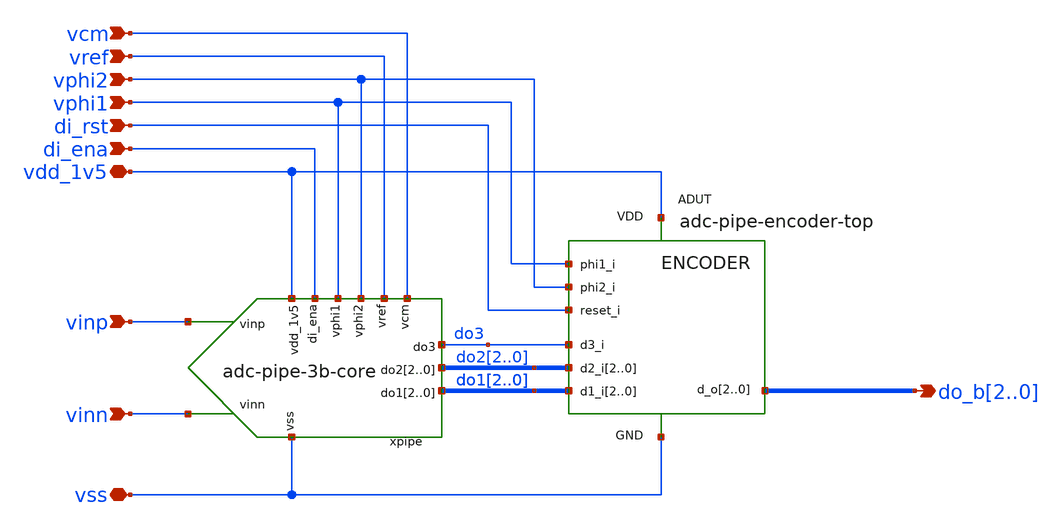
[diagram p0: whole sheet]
** sch_path: xschem/adc-pipe-3b-top.sch
* xschem/ota-5t-fd.sch:
* (c) 2025 M. Koefinger
**.subckt adc-pipe-3b-top vinp vinn di_rst di_ena vphi1 vphi2 vref vcm vdd_1v5 vss do_b2,do_b1,do_b0
*.ipin vinp
*.ipin vinn
*.ipin di_rst
*.ipin di_ena
*.ipin vphi1
*.ipin vphi2
*.ipin vref
*.ipin vcm
*.iopin vdd_1v5
*.iopin vss
*.opin do_b2,do_b1,do_b0
xpipe di_ena vphi2 vphi1 vcm vref vdd_1v5 vinp vinn do3 do22 do21 do20 do12 do11 do10 vss
+ adc-pipe-3b-core
ADUT [ vphi1 vphi2 di_rst do12 do11 do10 do22 do21 do20 do3 ] [ do_b2 do_b1 do_b0 ] encoder
**.ends

* expanding   symbol:  adc-pipe-3b-core.sym # of pins=12
** sym_path: xschem/adc-pipe-3b-core.sym
** sch_path: xschem/adc-pipe-3b-core.sch
.subckt adc-pipe-3b-core di_ena vphi2 vphi1 vcm vref vdd_1v5 vinp vinn do3 do22 do21 do20 do12 do11
+ do10 vss
*.iopin vdd_1v5
*.ipin vref
*.ipin vcm
*.ipin vphi1
*.ipin vphi2
*.ipin vinp
*.ipin vinn
*.iopin vss
*.ipin di_ena
*.opin do12,do11,do10
*.opin do22,do21,do20
*.opin do3
xmdac1 vdd_1v5 net1 vphi1 vphi2 vinp do12 do11 do10 vcm vss vres1p vcm vres1n vinn di_ena vss
+ mdac-tri-lvl
xadc1 do12 do11 do10 vinp vinn vref vcm vphi2 vss vphi1 adc-tri-lvl-ideal
xmdac2 vdd_1v5 net2 vphi2 vphi1 vres1p do22 do21 do20 vcm vss vres2p vcm vres2n vres1n di_ena vss
+ mdac-tri-lvl
xadc2 do22 do21 do20 vres1p vres1n vref vcm vphi1 vss vphi2 adc-tri-lvl-ideal
I0 vdd_1v5 net1 1.5u
I1 vdd_1v5 net2 1.5u
xadc3 do3 vres2p vres2n vcm vphi2 vss net3 vdd_1v5 vphi1 adc-1b-ideal
.ends


* expanding   symbol:  mdac-tri-lvl.sym # of pins=14
** sym_path: xschem/mdac-tri-lvl.sym
** sch_path: xschem/mdac-tri-lvl.sch
.subckt mdac-tri-lvl vdd_1v5 ibias_1u5 vhold vtrack vi_p di_code2 di_code1 di_code0 vref_p vref_n
+ vo_p vcm vo_n vi_n di_ena vss
*.ipin vi_p
*.ipin vi_n
*.ipin di_ena
*.iopin vss
*.iopin vdd_1v5
*.ipin ibias_1u5
*.opin vo_n
*.opin vo_p
*.ipin vref_p
*.ipin vref_n
*.ipin vcm
*.ipin di_code2,di_code1,di_code0
*.ipin vtrack
*.ipin vhold
xota vdd_1v5 vfb vo_p vo_n vgndp vgndn ibias_1u5 di_ena vss vbp ota-5t-fd
S1 vgndn vo_p vtrack vss SW1
xcmfb vhold vtrack vss vo_p vcm vbp vfb vo_n cmfb_sc cap={cap} div=10
S2 vgndp vo_n vtrack vss SW1
xc1 vhold vo_p vgndn vi_p vtrack vss sw_cap cap={cap} ron=1 roff=1G
xc2 vhold vdac_n vgndn vi_p vtrack vss sw_cap cap={cap} ron=1 roff=1G
xc3 vhold vo_n vgndp vi_n vtrack vss sw_cap cap={cap} ron=1 roff=1G
xc4 vhold vdac_p vgndp vi_n vtrack vss sw_cap cap={cap} ron=1 roff=1G
xsw1 di_code2 di_code1 di_code0 vref_p vref_n vdac_n vcm vss sw_dac ron=1 roff=1G
xsw2 di_code2 di_code1 di_code0 vref_n vref_p vdac_p vcm vss sw_dac ron=1 roff=1G
.ends


* expanding   symbol:  adc-tri-lvl-ideal.sym # of pins=8
** sym_path: xschem/adc-tri-lvl-ideal.sym
** sch_path: xschem/adc-tri-lvl-ideal.sch
.subckt adc-tri-lvl-ideal do[2] do[1] do[0] vip vin vref vcm vclk vss vclk_reg
*.iopin vss
*.ipin vip
*.ipin vin
*.ipin vref
*.ipin vcm
*.ipin vclk
*.opin do[2],do[1],do[0]
*.ipin vclk_reg
xcomp1 D1 vip vin vcm vref vss comp-macro
xcomp2 D0 vip vin vref vcm vss comp-macro
**** begin user architecture code


a31 Q_REG0 CLK_REG NULL NULL %d(Q0 NQ0) dff1
a32 Q_REG1 CLK_REG NULL NULL %d(Q1 NQ1) dff1


**** end user architecture code
**** begin user architecture code


.model adc_buf adc_bridge(in_low=0.7499 in_high=0.7501)
.model dac1 dac_bridge(out_low = 0 out_high = 1.5 out_undef = 0 input_load = 0.1e-15 t_rise =
+ 0.01e-9 t_fall = 0.01e-9)
.model inv1 d_inverter(rise_delay = 0.01e-9 fall_delay = 0.01e-9 input_load = 0.1e-15)
.model and1 d_and(rise_delay = 0.01e-9 fall_delay = 0.01e-9 input_load = 0.01e-15)
.model dff1 d_dff(clk_delay = 0.01e-9 set_delay = 0.01e-9 reset_delay = 0.01e-9 ic = 0 rise_delay =
+ 0.01e-9 fall_delay = 0.01e-9)
.model dlatch1 d_dlatch(data_delay = 0.01e-9 enable_delay = 0.01e-9 set_delay = 0.01e-9 reset_delay
+ = 0.01e-9 ic = 0 rise_delay = 0.01e-9 fall_delay = 0.01e-9)

**** end user architecture code
A1 [ vclk ] [ CLK ] adc_buf
A3 [ H1 ] [ do1 ] dac1
A4 [ H2 ] [ do2 ] dac1
**** begin user architecture code


a23 [NQ1 Q0] %d(H0) and1
a24 [NQ1 NQ0] %d(H1) and1
a25 [Q1 Q0] %d(H2) and1


**** end user architecture code
A2 [ H0 ] [ do0 ] dac1
V1 do2 do[2] 0
V2 do1 do[1] 0
V3 do0 do[0] 0
**** begin user architecture code


a21 D0 CLK NULL NULL %d(Q_REG0 NQ_REG0) dlatch1
a22 D1 CLK NULL NULL %d(Q_REG1 NQ_REG1) dlatch1


**** end user architecture code
A5 [ vclk_reg ] [ CLK_REG ] adc_buf
.ends


* expanding   symbol:  adc-1b-ideal.sym # of pins=9
** sym_path: xschem/legacy/adc-1b-ideal.sym
** sch_path: xschem/legacy/adc-1b-ideal.sch
.subckt adc-1b-ideal do vip vin vcm vclk vss do_b vdd vclk_reg
*.iopin vss
*.ipin vip
*.ipin vin
*.ipin vcm
*.ipin vclk
*.opin do_b
*.opin do
*.iopin vdd
*.ipin vclk_reg
**** begin user architecture code


.model adc_buf adc_bridge(in_low=0.7499 in_high=0.7501)
.model dac1 dac_bridge(out_low = 0 out_high = 1.5 out_undef = 0 input_load = 0.1e-15 t_rise =
+ 0.01e-9 t_fall = 0.01e-9)
.model nor1 d_nor(rise_delay = 0.01e-9 fall_delay = 0.01e-9 input_load = 0.01e-15)
.model dlatch1 d_dlatch(data_delay = 0.01e-9 enable_delay = 0.01e-9 set_delay = 0.01e-9 reset_delay
+ = 0.01e-9 ic = 0 rise_delay = 0.01e-9 fall_delay = 0.01e-9)
.model dff1 d_dff(clk_delay = 0.01e-9 set_delay = 0.01e-9 reset_delay = 0.01e-9 ic = 0 rise_delay =
+ 0.01e-9 fall_delay = 0.01e-9)


**** end user architecture code
A3 [ NQ1 ] [ do_b ] dac1
A2 [ Q1 ] [ do ] dac1
**** begin user architecture code


a21 [D0 NQ0] Q0 nor1
a22 [ND0 Q0] NQ0 nor1


**** end user architecture code
xcomp vdd vclk ND0 D0 vin vcm vcm vip vss sal-macro
**** begin user architecture code


a23 Q0 CLK NULL NULL %d(Q_REG0 NULL) dlatch1
a24 NQ0 CLK NULL NULL %d(NQ_REG0 NULL) dlatch1


**** end user architecture code
A1 [ vclk ] [ CLK ] adc_buf
**** begin user architecture code


a31 Q_REG0 CLK_REG NULL NULL %d(Q1 NULL) dff1
a32 NQ_REG0 CLK_REG NULL NULL %d(NQ1 NULL) dff1


**** end user architecture code
A4 [ vclk_reg ] [ CLK_REG ] adc_buf
.ends


* expanding   symbol:  ota-5t-fd.sym # of pins=10
** sym_path: xschem/ota-5t-fd.sym
** sch_path: xschem/ota-5t-fd.sch
.subckt ota-5t-fd vdd vfb voutp voutn vinp vinn ibias_1u5 d_ena vss vbp
*.ipin ibias_1u5
*.iopin vdd
*.iopin vss
*.ipin vinp
*.ipin vinn
*.opin voutn
*.ipin d_ena
*.opin voutp
*.ipin vfb
*.opin vbp
XMN3 tail gate_n vss vss sg13_lv_nmos w=2.5u l=0.5u ng=5 m=1 mm_ok=1
XMP2 voutp vfb vdd vdd sg13_lv_pmos w=0.5u l=0.5u ng=1 m=1 mm_ok=1
XMN1 voutn vinp tail vss sg13_lv_nmos w=5.5u l=0.5u ng=11 m=1 mm_ok=1
XMN2 voutp vinn tail vss sg13_lv_nmos w=5.5u l=0.5u ng=11 m=1 mm_ok=1
XMP1 voutn vfb vdd vdd sg13_lv_pmos w=0.5u l=0.5u ng=1 m=1 mm_ok=1
XMN4 ibias_1u5 gate_n vss vss sg13_lv_nmos w=1.5u l=0.5u ng=3 m=1 mm_ok=1
XMN5 gate_n ena_n vss vss sg13_lv_nmos w=0.5u l=0.13u ng=1 m=1 mm_ok=1
XMPSW1 vfb ena vdd vdd sg13_lv_pmos w=1.5u l=0.13u ng=1 m=1 mm_ok=1
XMN8 ena ena_n vss vss sg13_lv_nmos w=0.5u l=0.13u ng=1 m=1 mm_ok=1
XMP5 ena ena_n vdd vdd sg13_lv_pmos w=1.5u l=0.13u ng=1 m=1 mm_ok=1
XMN6 ibias_1u5 ena gate_n vss sg13_lv_nmos w=0.5u l=0.13u ng=1 m=1 mm_ok=1
XMN7 ena_n d_ena vss vss sg13_lv_nmos w=0.5u l=0.13u ng=1 m=1 mm_ok=1
XMP4 ena_n d_ena vdd vdd sg13_lv_pmos w=1.5u l=0.13u ng=1 m=1 mm_ok=1
XMN9 vbp gate_n vss vss sg13_lv_nmos w=1u l=0.5u ng=2 m=1 mm_ok=1
XMP3 vbp vbp vdd vdd sg13_lv_pmos w=0.5u l=0.5u ng=1 m=1 mm_ok=1
.ends


* expanding   symbol:  cmfb_sc.sym # of pins=8
** sym_path: xschem/cmfb_sc.sym
** sch_path: xschem/cmfb_sc.sch
.subckt cmfb_sc vphi2 vphi1 vss vo_p vcm vbias vfb vo_n  cap=100f div=10
*.ipin vcm
*.ipin vphi2
*.ipin vphi1
*.iopin vss
*.ipin vbias
*.iopin vo_p
*.iopin vo_n
*.opin vfb
C1 vo_p vfb 100f m=1
C2 net1 net2 10f m=1
C3 vfb vo_n 100f m=1
C4 net2 net3 10f m=1
S3 net1 vo_p vphi1 vss SW1
S4 vcm net1 vphi2 vss SW1
S6 net2 vfb vphi1 vss SW1
S7 vbias net2 vphi2 vss SW1
S9 net3 vo_n vphi1 vss SW1
S10 vcm net3 vphi2 vss SW1
.ends


* expanding   symbol:  sw_cap.sym # of pins=6
** sym_path: xschem/sw_cap.sym
** sch_path: xschem/sw_cap.sch
.subckt sw_cap di_1 vi1 vo vi2 di_2 vss  cap=100f ron=1 roff=1G
*.ipin di_1
*.ipin di_2
*.iopin vi1
*.iopin vi2
*.iopin vo
*.iopin vss
C1 vc_p vo {cap} m=1
S1 vi1 vc_p di_1 vss SW1
S2 vi2 vc_p di_2 vss SW1
.ends


* expanding   symbol:  sw_dac.sym # of pins=6
** sym_path: xschem/sw_dac.sym
** sch_path: xschem/sw_dac.sch
.subckt sw_dac di_code2 di_code1 di_code0 vref_p vref_n vo vcm vss  ron=1 roff=1G
*.ipin di_code2,di_code1,di_code0
*.iopin vref_p
*.iopin vref_n
*.iopin vo
*.iopin vss
*.iopin vcm
S1 vref_p vo di_code2 vss SW1
S2 vref_n vo di_code1 vss SW1
S3 vcm vo di_code0 vss SW1
.ends


* expanding   symbol:  comp-macro.sym # of pins=6
** sym_path: xschem/comp-macro.sym
** sch_path: xschem/comp-macro.sch
.subckt comp-macro do vip_1 vin_1 vip_2 vin_2 vss
*.iopin vss
*.ipin vip_1
*.ipin vin_1
*.ipin vip_2
*.ipin vin_2
*.opin do
A1 [ net1 ] [ net2 ] comp0
E1 net1 net3 vip_1 vin_1 1
E2 net3 vss vip_2 vin_2 1
**** begin user architecture code


.model comp0 adc_bridge(in_low=-0.0001 in_high=0.0001)
.model dac1 dac_bridge(out_low = 0 out_high = 1.5 out_undef = 0 input_load = 0.1e-15 t_rise =
+ 0.01e-9 t_fall = 0.01e-9)


**** end user architecture code
A2 [ net2 ] [ do ] dac1
.ends


* expanding   symbol:  sal-macro.sym # of pins=9
** sym_path: xschem/sal-macro.sym
** sch_path: xschem/sal-macro.sch
.subckt sal-macro vdd vclk do_b do vin_1 vip_2 vin_2 vip_1 vss
*.iopin vss
*.ipin vip_1
*.ipin vip_2
*.ipin vin_2
*.opin do
*.ipin vin_1
*.iopin vdd
*.opin do_b
*.ipin vclk
A1 [ net5 ] [ do ] comp0
G1 net2 net1 vip_1 net1 10e-6
**** begin user architecture code

.model comp0 adc_bridge(in_low=0.74 in_high=0.76)

**** end user architecture code
G3 net3 net1 vin_1 net1 10e-6
S1 net1 vss vclk vss SW1
G2 net5 net3 net4 net3 10e-6
G4 net4 net2 net5 net2 10e-6
G5 vdd net5 vdd net4 10e-6
G6 vdd net4 vdd net5 10e-6
S3 vdd net4 vdd vclk SW1
S4 vdd net2 vdd vclk SW1
S5 vdd net5 vdd vclk SW1
S6 vdd net2 vdd vclk SW1
A2 [ net4 ] [ do_b ] comp0
R1 vdd net4 1Meg m=1
R2 vdd net5 1Meg m=1
R3 net5 net3 1Meg m=1
R4 net4 net2 1Meg m=1
R5 net2 net1 100Meg m=1
R6 net3 net1 100e-6 m=1
.ends

**** begin user architecture code
.MODEL SW1 SW( VT=0.75 VH=0.01 RON=1 ROFF=100Meg )
.model encoder d_cosim simulation="../verilog/rtl/adc_pipe_encoder_TOP.so"
**** end user architecture code
.end
